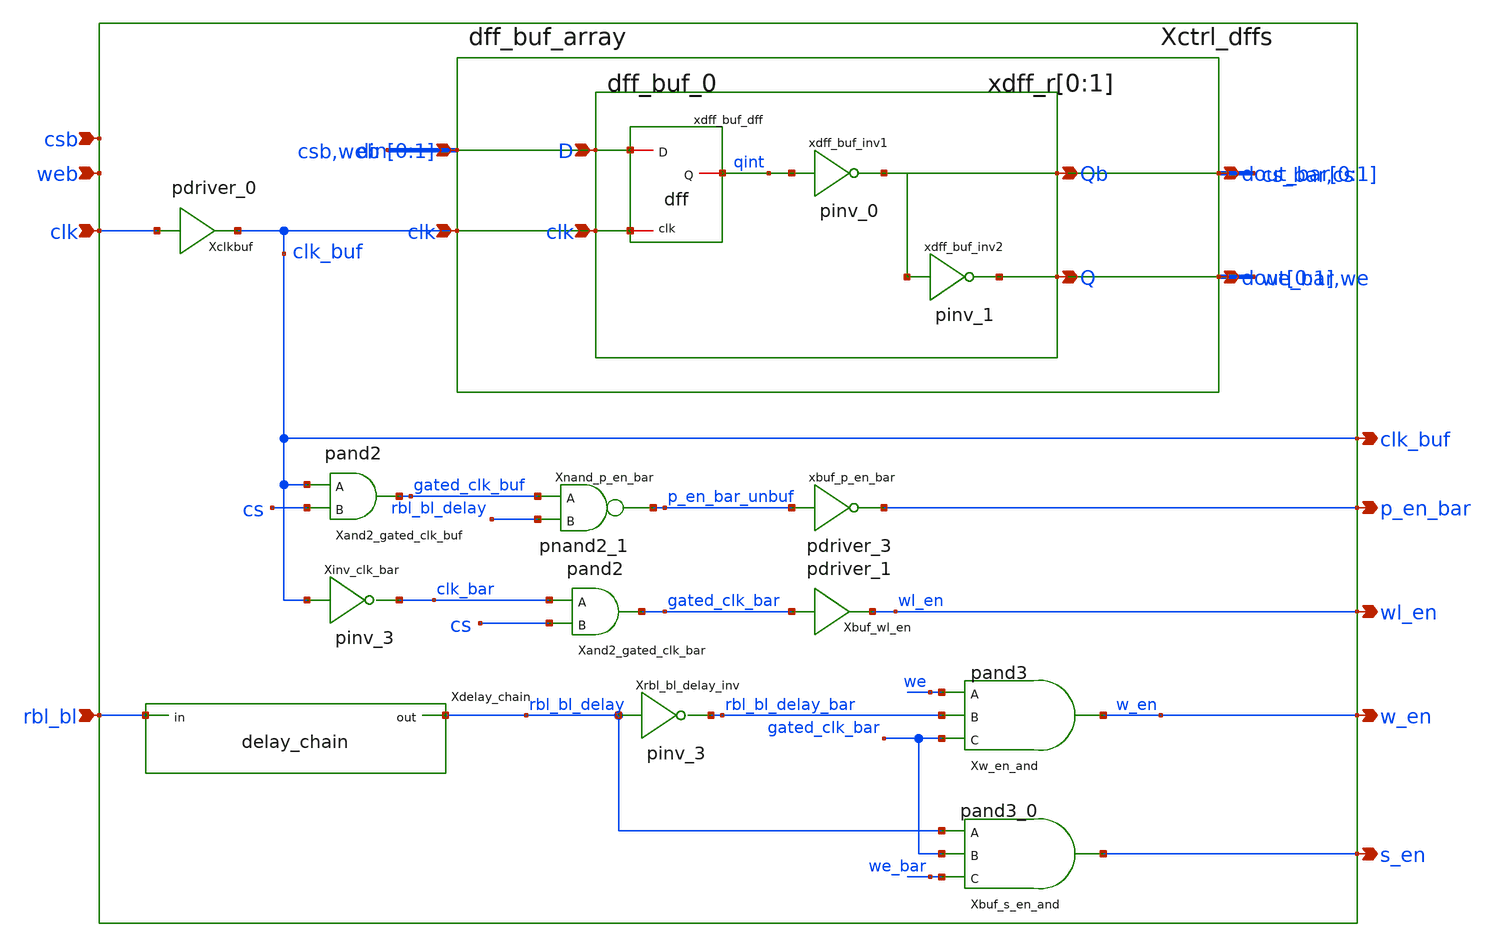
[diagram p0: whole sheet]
** sch_path: sram_4_16_scn4m/control_logic_rw.sch
**.subckt control_logic_rw clk rbl_bl s_en w_en p_en_bar wl_en csb web clk_buf
*.ipin clk
*.ipin rbl_bl
*.opin s_en
*.opin w_en
*.opin p_en_bar
*.opin wl_en
*.ipin csb
*.ipin web
*.opin clk_buf
Xclkbuf clk clk_buf vdd gnd pdriver_0
Xinv_clk_bar clk_buf clk_bar vdd gnd pinv_3
Xand2_gated_clk_bar clk_bar cs gated_clk_bar vdd gnd pand2
Xand2_gated_clk_buf clk_buf cs gated_clk_buf vdd gnd pand2
Xbuf_wl_en gated_clk_bar wl_en vdd gnd pdriver_1
Xrbl_bl_delay_inv rbl_bl_delay rbl_bl_delay_bar vdd gnd pinv_3
Xw_en_and we rbl_bl_delay_bar gated_clk_bar w_en vdd gnd pand3
Xbuf_s_en_and rbl_bl_delay gated_clk_bar we_bar s_en vdd gnd pand3_0
Xdelay_chain rbl_bl rbl_bl_delay vdd gnd delay_chain
Xnand_p_en_bar gated_clk_buf rbl_bl_delay p_en_bar_unbuf vdd gnd pnand2_1
xbuf_p_en_bar p_en_bar_unbuf p_en_bar vdd gnd pdriver_3
Xctrl_dffs csb web we_bar we cs_bar cs clk_buf vdd gnd dff_buf_array
**.ends
.end
